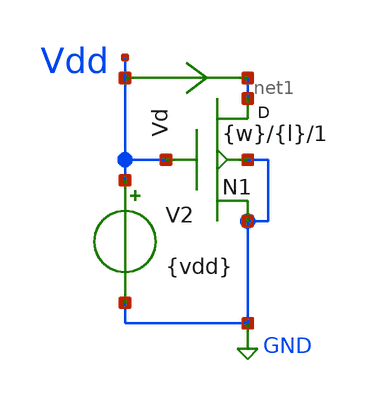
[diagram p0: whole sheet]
** sch_path: Parametros_Vaf/zeta_test.sch
**.subckt zeta_test
N1 net1 Vdd GND GND NMOS_ACM w={w} l={l} m=1
V2 Vdd GND {vdd}
Vd Vdd net1 0
.save i(vd)
**** begin user architecture code


* Circuit Parameters
.param vdd = 1.2
.param w = 5.0u
.param l = 0.18u
* Include Models
.model NMOS_ACM nmos_ACM
.model PMOS_ACM pmos_ACM
* OP Parameters & Singals to save
.save all
*Simulations
.op
.control
pre_osdi NMOS_ACM_2V0.osdi
pre_osdi PMOS_ACM_2V0.osdi
run
print i(Vd)
set filetype = ascii
write dcsweep.raw
.endc
.end


**** end user architecture code
**.ends
.GLOBAL GND
.end
